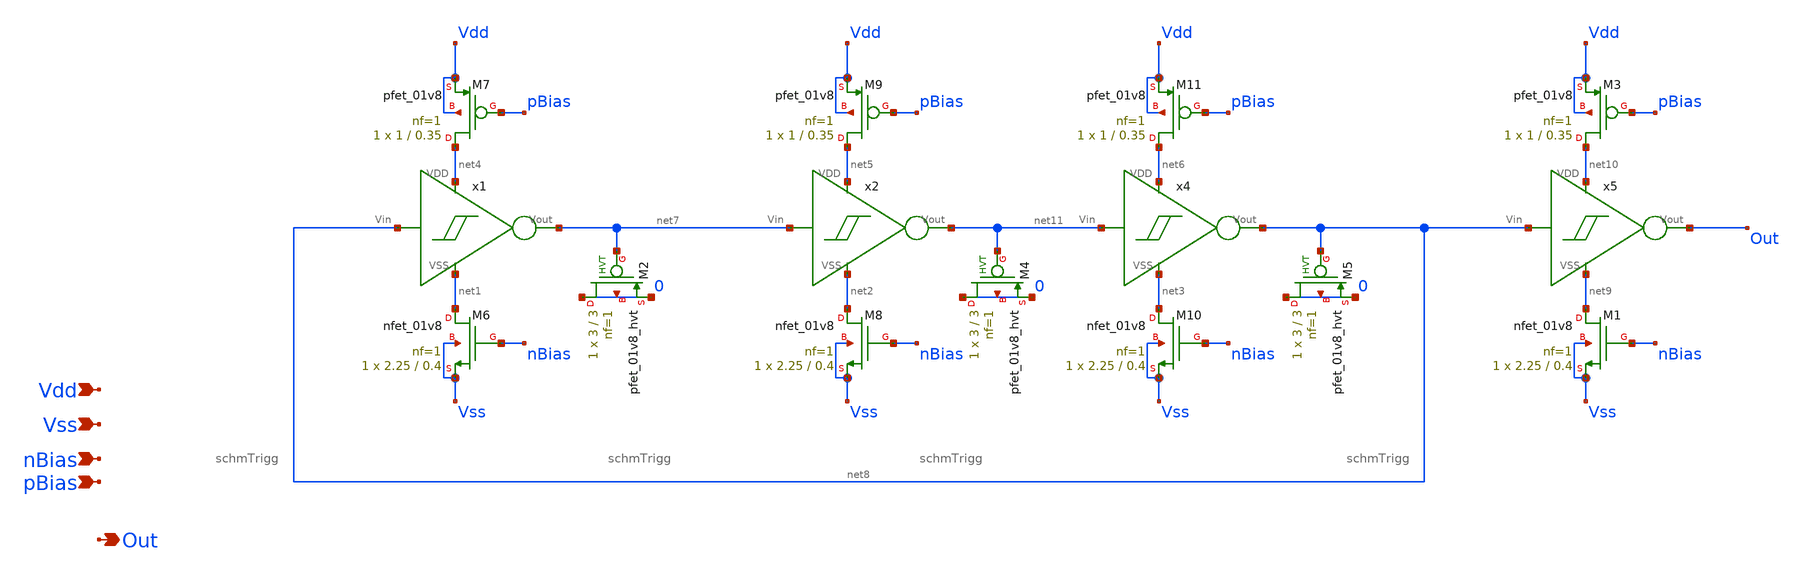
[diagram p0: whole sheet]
** sch_path: xschem/T3/oscillators/A_tt10_Ring_currentStarved/osc.sch
**.subckt osc Vdd Vss Out nBias pBias
*.ipin Vdd
*.ipin Vss
*.opin Out
*.ipin nBias
*.ipin pBias
XM6 net1 nBias Vss Vss sky130_fd_pr__nfet_01v8 L=0.4 W=2.25 nf=1 ad='int((1 + 1)/2) * 2.25 / 1 * 0.29'
+ as='int((1 + 2)/2) * 2.25 / 1 * 0.29' pd='2*int((1 + 1)/2) * (2.25 / 1 + 0.29)' ps='2*int((1 + 2)/2) * (2.25 / 1 + 0.29)'
+ nrd='0.29 / 2.25 ' nrs='0.29 / 2.25 ' sa=0 sb=0 sd=0 mult=1 m=1
XM7 net4 pBias Vdd Vdd sky130_fd_pr__pfet_01v8 L=0.35 W=1 nf=1 ad='int((nf+1)/2) * W/nf * 0.29' as='int((nf+2)/2) * W/nf * 0.29'
+ pd='2*int((nf+1)/2) * (W/nf + 0.29)' ps='2*int((nf+2)/2) * (W/nf + 0.29)' nrd='0.29 / W' nrs='0.29 / W'
+ sa=0 sb=0 sd=0 mult=1 m=1
XM8 net2 nBias Vss Vss sky130_fd_pr__nfet_01v8 L=0.4 W=2.25 nf=1 ad='int((1 + 1)/2) * 2.25 / 1 * 0.29'
+ as='int((1 + 2)/2) * 2.25 / 1 * 0.29' pd='2*int((1 + 1)/2) * (2.25 / 1 + 0.29)' ps='2*int((1 + 2)/2) * (2.25 / 1 + 0.29)'
+ nrd='0.29 / 2.25 ' nrs='0.29 / 2.25 ' sa=0 sb=0 sd=0 mult=1 m=1
XM9 net5 pBias Vdd Vdd sky130_fd_pr__pfet_01v8 L=0.35 W=1 nf=1 ad='int((nf+1)/2) * W/nf * 0.29' as='int((nf+2)/2) * W/nf * 0.29'
+ pd='2*int((nf+1)/2) * (W/nf + 0.29)' ps='2*int((nf+2)/2) * (W/nf + 0.29)' nrd='0.29 / W' nrs='0.29 / W'
+ sa=0 sb=0 sd=0 mult=1 m=1
XM10 net3 nBias Vss Vss sky130_fd_pr__nfet_01v8 L=0.4 W=2.25 nf=1 ad='int((1 + 1)/2) * 2.25 / 1 * 0.29'
+ as='int((1 + 2)/2) * 2.25 / 1 * 0.29' pd='2*int((1 + 1)/2) * (2.25 / 1 + 0.29)' ps='2*int((1 + 2)/2) * (2.25 / 1 + 0.29)'
+ nrd='0.29 / 2.25 ' nrs='0.29 / 2.25 ' sa=0 sb=0 sd=0 mult=1 m=1
XM11 net6 pBias Vdd Vdd sky130_fd_pr__pfet_01v8 L=0.35 W=1 nf=1 ad='int((nf+1)/2) * W/nf * 0.29' as='int((nf+2)/2) * W/nf * 0.29'
+ pd='2*int((nf+1)/2) * (W/nf + 0.29)' ps='2*int((nf+2)/2) * (W/nf + 0.29)' nrd='0.29 / W' nrs='0.29 / W'
+ sa=0 sb=0 sd=0 mult=1 m=1
x2 net7 net2 net5 net11 schmTrigg
x1 net8 net1 net4 net7 schmTrigg
x4 net11 net3 net6 net8 schmTrigg
XM1 net9 nBias Vss Vss sky130_fd_pr__nfet_01v8 L=0.4 W=2.25 nf=1 ad='int((1 + 1)/2) * 2.25 / 1 * 0.29'
+ as='int((1 + 2)/2) * 2.25 / 1 * 0.29' pd='2*int((1 + 1)/2) * (2.25 / 1 + 0.29)' ps='2*int((1 + 2)/2) * (2.25 / 1 + 0.29)'
+ nrd='0.29 / 2.25 ' nrs='0.29 / 2.25 ' sa=0 sb=0 sd=0 mult=1 m=1
XM3 net10 pBias Vdd Vdd sky130_fd_pr__pfet_01v8 L=0.35 W=1 nf=1 ad='int((nf+1)/2) * W/nf * 0.29' as='int((nf+2)/2) * W/nf * 0.29'
+ pd='2*int((nf+1)/2) * (W/nf + 0.29)' ps='2*int((nf+2)/2) * (W/nf + 0.29)' nrd='0.29 / W' nrs='0.29 / W'
+ sa=0 sb=0 sd=0 mult=1 m=1
x5 net8 net9 net10 Out schmTrigg
XM5 0 net8 0 0 sky130_fd_pr__pfet_01v8_hvt L=3 W=3 nf=1 ad='int((1 + 1)/2) * 3 / 1 * 0.29' as='int((1 + 2)/2) * 3 / 1 * 0.29'
+ pd='2*int((1 + 1)/2) * (3 / 1 + 0.29)' ps='2*int((1 + 2)/2) * (3 / 1 + 0.29)' nrd='0.29 / 3 ' nrs='0.29 / 3 '
+ sa=0 sb=0 sd=0 mult=1 m=1
XM2 0 net7 0 0 sky130_fd_pr__pfet_01v8_hvt L=3 W=3 nf=1 ad='int((1 + 1)/2) * 3 / 1 * 0.29' as='int((1 + 2)/2) * 3 / 1 * 0.29'
+ pd='2*int((1 + 1)/2) * (3 / 1 + 0.29)' ps='2*int((1 + 2)/2) * (3 / 1 + 0.29)' nrd='0.29 / 3 ' nrs='0.29 / 3 '
+ sa=0 sb=0 sd=0 mult=1 m=1
XM4 0 net11 0 0 sky130_fd_pr__pfet_01v8_hvt L=3 W=3 nf=1 ad='int((1 + 1)/2) * 3 / 1 * 0.29' as='int((1 + 2)/2) * 3 / 1 * 0.29'
+ pd='2*int((1 + 1)/2) * (3 / 1 + 0.29)' ps='2*int((1 + 2)/2) * (3 / 1 + 0.29)' nrd='0.29 / 3 ' nrs='0.29 / 3 '
+ sa=0 sb=0 sd=0 mult=1 m=1
**.ends

* expanding   symbol:  T1/schmTrigg/schmTrigg.sym # of pins=4
** sym_path: xschem/T1/schmTrigg/schmTrigg.sym
** sch_path: xschem/T1/schmTrigg/schmTrigg.sch
.subckt schmTrigg Vin VSS VDD Vout
*.ipin Vin
*.ipin VDD
*.ipin VSS
*.opin Vout
XM1 VDD Vout Vn Vn sky130_fd_pr__nfet_01v8 L=0.15 W=1 nf=1 ad='int((1 + 1)/2) * 1 / 1 * 0.29' as='int((1 + 2)/2) * 1 / 1 * 0.29'
+ pd='2*int((1 + 1)/2) * (1 / 1 + 0.29)' ps='2*int((1 + 2)/2) * (1 / 1 + 0.29)' nrd='0.29 / 1 ' nrs='0.29 / 1 '
+ sa=0 sb=0 sd=0 mult=1 m=1
XM2 Vn Vin VSS VSS sky130_fd_pr__nfet_01v8 L=0.15 W=1 nf=1 ad='int((1 + 1)/2) * 1 / 1 * 0.29' as='int((1 + 2)/2) * 1 / 1 * 0.29'
+ pd='2*int((1 + 1)/2) * (1 / 1 + 0.29)' ps='2*int((1 + 2)/2) * (1 / 1 + 0.29)' nrd='0.29 / 1 ' nrs='0.29 / 1 '
+ sa=0 sb=0 sd=0 mult=1 m=1
XM3 Vout Vin Vn Vn sky130_fd_pr__nfet_01v8 L=0.15 W=1 nf=1 ad='int((1 + 1)/2) * 1 / 1 * 0.29' as='int((1 + 2)/2) * 1 / 1 * 0.29'
+ pd='2*int((1 + 1)/2) * (1 / 1 + 0.29)' ps='2*int((1 + 2)/2) * (1 / 1 + 0.29)' nrd='0.29 / 1 ' nrs='0.29 / 1 '
+ sa=0 sb=0 sd=0 mult=1 m=1
XM4 VSS Vout Vp Vp sky130_fd_pr__pfet_01v8 L=0.15 W=1 nf=1 ad='int((nf+1)/2) * W/nf * 0.29' as='int((nf+2)/2) * W/nf * 0.29'
+ pd='2*int((nf+1)/2) * (W/nf + 0.29)' ps='2*int((nf+2)/2) * (W/nf + 0.29)' nrd='0.29 / W' nrs='0.29 / W'
+ sa=0 sb=0 sd=0 mult=1 m=1
XM5 Vout Vin Vp Vp sky130_fd_pr__pfet_01v8 L=0.15 W=1 nf=1 ad='int((nf+1)/2) * W/nf * 0.29' as='int((nf+2)/2) * W/nf * 0.29'
+ pd='2*int((nf+1)/2) * (W/nf + 0.29)' ps='2*int((nf+2)/2) * (W/nf + 0.29)' nrd='0.29 / W' nrs='0.29 / W'
+ sa=0 sb=0 sd=0 mult=1 m=1
XM6 Vp Vin VDD VDD sky130_fd_pr__pfet_01v8 L=0.15 W=1 nf=1 ad='int((nf+1)/2) * W/nf * 0.29' as='int((nf+2)/2) * W/nf * 0.29'
+ pd='2*int((nf+1)/2) * (W/nf + 0.29)' ps='2*int((nf+2)/2) * (W/nf + 0.29)' nrd='0.29 / W' nrs='0.29 / W'
+ sa=0 sb=0 sd=0 mult=1 m=1
.ends

.end
